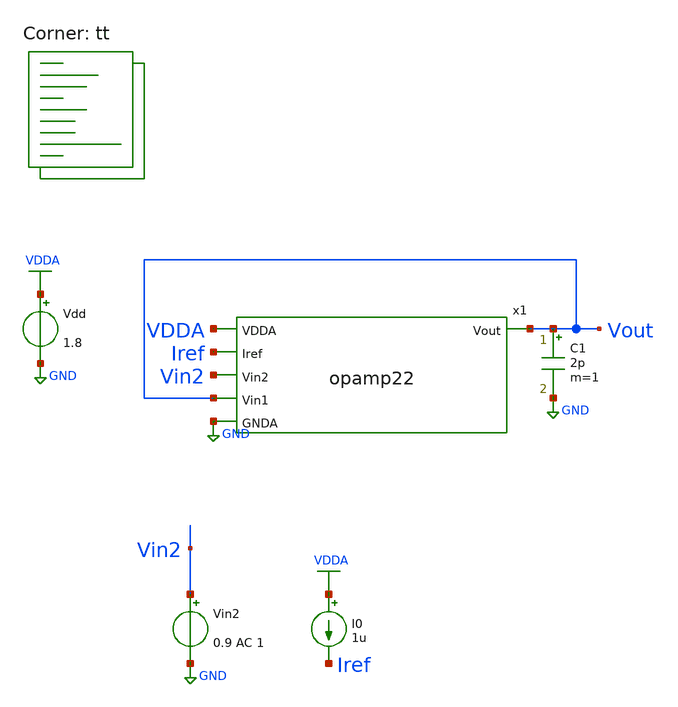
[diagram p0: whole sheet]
** sch_path: projects/pll/trials/tb_opamp22.sch
**.subckt tb_opamp22
x1 VDDA Iref Vin2 Vout Vout GND opamp22
Vdd VDDA GND 1.8
Vin2 Vin2 GND 0.9 AC 1
I0 VDDA Iref 1u
C1 Vout GND 2p m=1
**** begin user architecture code



.option wnflag=1

.control

  save all
  ac dec 20 1 1e12
  * dc Vin2 0 1.8 0.01
  let Tmag = db(v(Vout))
  let Tphase = 180*cph(v(Vout))/pi
  write tb_opamp22.raw
  set appendwrite

.endc



.lib $::SKYWATER_MODELS/sky130.lib.spice tt
**** end user architecture code
**.ends

* expanding   symbol:  /foss/designs/my_design/projects/pll/trials/opamp22.sym # of pins=6
** sym_path: projects/pll/trials/opamp22.sym
** sch_path: projects/pll/trials/opamp22.sch
.subckt opamp22 VDDA Iref Vin2 Vin1 Vout GNDA
*.ipin Iref
*.opin Vout
*.ipin Vin2
*.ipin Vin1
*.ipin VDDA
*.ipin GNDA
XM1 net1 net2 VDDA VDD sky130_fd_pr__pfet_01v8 L=0.15 W=4 nf=1 ad='int((nf+1)/2) * W/nf * 0.29' as='int((nf+2)/2) * W/nf * 0.29'
+ pd='2*int((nf+1)/2) * (W/nf + 0.29)' ps='2*int((nf+2)/2) * (W/nf + 0.29)' nrd='0.29 / W' nrs='0.29 / W'
+ sa=0 sb=0 sd=0 mult=1 m=1
XM2 net1 Vin2 net3 GND sky130_fd_pr__nfet_01v8 L=0.15 W=2 nf=1 ad='int((nf+1)/2) * W/nf * 0.29' as='int((nf+2)/2) * W/nf * 0.29'
+ pd='2*int((nf+1)/2) * (W/nf + 0.29)' ps='2*int((nf+2)/2) * (W/nf + 0.29)' nrd='0.29 / W' nrs='0.29 / W'
+ sa=0 sb=0 sd=0 mult=1 m=1
XM3 net2 Vin1 net3 GND sky130_fd_pr__nfet_01v8 L=0.15 W=2 nf=1 ad='int((nf+1)/2) * W/nf * 0.29' as='int((nf+2)/2) * W/nf * 0.29'
+ pd='2*int((nf+1)/2) * (W/nf + 0.29)' ps='2*int((nf+2)/2) * (W/nf + 0.29)' nrd='0.29 / W' nrs='0.29 / W'
+ sa=0 sb=0 sd=0 mult=1 m=1
XM4 net2 net2 VDDA VDD sky130_fd_pr__pfet_01v8 L=0.15 W=4 nf=1 ad='int((nf+1)/2) * W/nf * 0.29' as='int((nf+2)/2) * W/nf * 0.29'
+ pd='2*int((nf+1)/2) * (W/nf + 0.29)' ps='2*int((nf+2)/2) * (W/nf + 0.29)' nrd='0.29 / W' nrs='0.29 / W'
+ sa=0 sb=0 sd=0 mult=1 m=1
XM5 Vout Iref GNDA GND sky130_fd_pr__nfet_01v8 L=0.15 W=4 nf=1 ad='int((nf+1)/2) * W/nf * 0.29' as='int((nf+2)/2) * W/nf * 0.29'
+ pd='2*int((nf+1)/2) * (W/nf + 0.29)' ps='2*int((nf+2)/2) * (W/nf + 0.29)' nrd='0.29 / W' nrs='0.29 / W'
+ sa=0 sb=0 sd=0 mult=1 m=1
XM6 Vout net1 VDDA VDD sky130_fd_pr__pfet_01v8 L=0.15 W=4 nf=1 ad='int((nf+1)/2) * W/nf * 0.29' as='int((nf+2)/2) * W/nf * 0.29'
+ pd='2*int((nf+1)/2) * (W/nf + 0.29)' ps='2*int((nf+2)/2) * (W/nf + 0.29)' nrd='0.29 / W' nrs='0.29 / W'
+ sa=0 sb=0 sd=0 mult=1 m=1
XM7 net3 Iref GNDA GND sky130_fd_pr__nfet_01v8 L=0.15 W=4 nf=1 ad='int((nf+1)/2) * W/nf * 0.29' as='int((nf+2)/2) * W/nf * 0.29'
+ pd='2*int((nf+1)/2) * (W/nf + 0.29)' ps='2*int((nf+2)/2) * (W/nf + 0.29)' nrd='0.29 / W' nrs='0.29 / W'
+ sa=0 sb=0 sd=0 mult=1 m=1
XM9 Iref Iref GNDA GND sky130_fd_pr__nfet_01v8 L=0.15 W=1 nf=1 ad='int((nf+1)/2) * W/nf * 0.29' as='int((nf+2)/2) * W/nf * 0.29'
+ pd='2*int((nf+1)/2) * (W/nf + 0.29)' ps='2*int((nf+2)/2) * (W/nf + 0.29)' nrd='0.29 / W' nrs='0.29 / W'
+ sa=0 sb=0 sd=0 mult=1 m=1
.ends

.GLOBAL GND
.GLOBAL VDDA
.end
